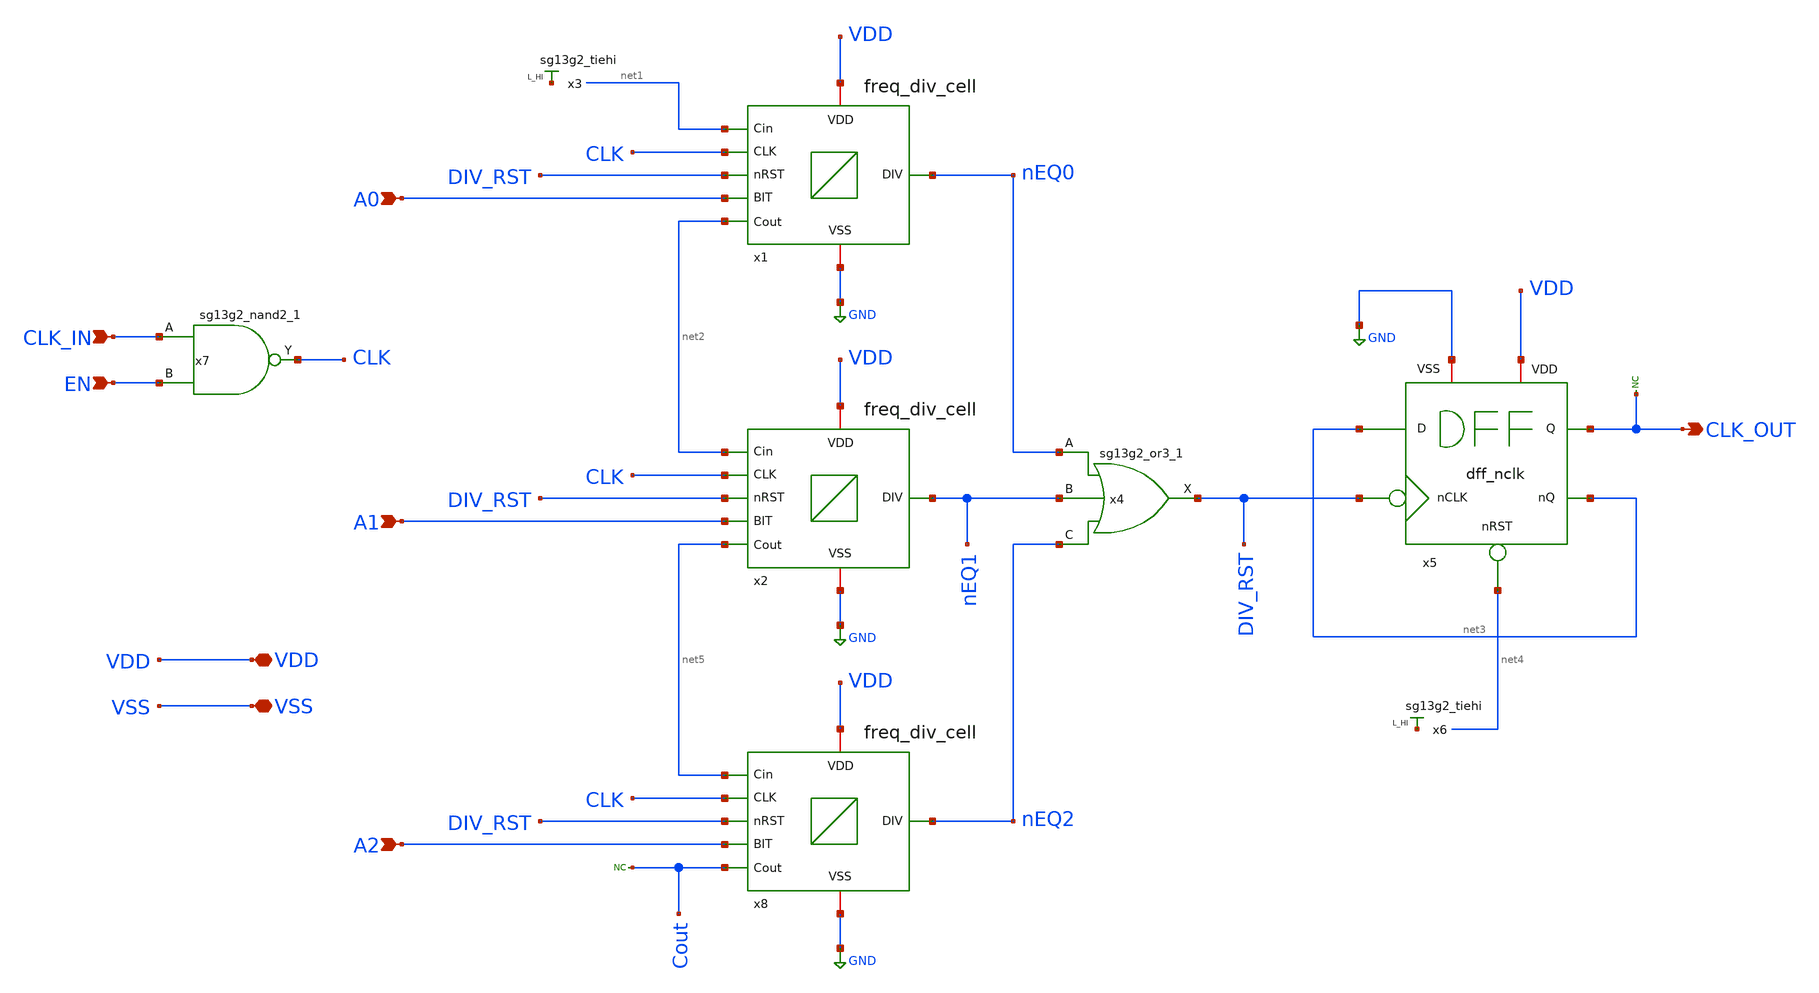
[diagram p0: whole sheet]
** sch_path: Combined Design/design_data/xschem/3bit_freq_divider.sch
* IHP-GmbH/IHP-Open-PDK/ihp-sg13g2/libs.tech/xschem/sg13g2_stdcells/sg13g2_or3_1.sch:
* Copyright 2023 IHP PDK Authors
* Licensed under the Apache License, Version 2.0 (the "License");
**.subckt 3bit_freq_divider CLK_IN EN A0 A1 CLK_OUT VSS VDD A2
*.ipin CLK_IN
*.ipin EN
*.ipin A0
*.ipin A1
*.opin CLK_OUT
*.iopin VSS
*.iopin VDD
*.ipin A2
x1 VDD GND nEQ0 net1 CLK net2 DIV_RST A0 freq_div_cell
x2 VDD GND nEQ1 net2 CLK net5 DIV_RST A1 freq_div_cell
x3 net6 VDD VSS sg13g2_tiehi
x5 DIV_RST CLK_OUT net3 net3 net4 VDD GND dff_nclk
x6 net7 VDD VSS sg13g2_tiehi
* noconn CLK_OUT
x7 CLK CLK_IN EN VDD VSS sg13g2_nand2_1
x4 DIV_RST nEQ0 nEQ1 nEQ2 VDD VSS sg13g2_or3_1
x8 VDD GND nEQ2 net5 CLK Cout DIV_RST A2 freq_div_cell
* noconn Cout
**.ends

* expanding   symbol:  sg13g2_stdcells/sg13g2_nand2_1.sym # of pins=3
** sym_path: sg13g2_stdcells/sg13g2_nand2_1.sym
** sch_path: sg13g2_stdcells/sg13g2_nand2_1.sch
.subckt sg13g2_nand2_1 Y A B VDD VSS
*.iopin VDD
*.iopin VSS
*.ipin A
*.ipin B
*.opin Y
XM1 Y A net1 VSS sg13_lv_nmos w=740.00n l=130.00n ng=1 m=1 mm_ok=1
XM2 net1 B VSS VSS sg13_lv_nmos w=740.00n l=130.00n ng=1 m=1 mm_ok=1
XM3 Y A VDD VDD sg13_lv_pmos w=1.12u l=130.00n ng=1 m=1 mm_ok=1
XM4 Y B VDD VDD sg13_lv_pmos w=1.12u l=130.00n ng=1 m=1 mm_ok=1
.ends


* expanding   symbol:  sg13g2_stdcells/sg13g2_or3_1.sym # of pins=4
** sym_path: sg13g2_stdcells/sg13g2_or3_1.sym
** sch_path: sg13g2_stdcells/sg13g2_or3_1.sch
.subckt sg13g2_or3_1 X A B C VDD VSS
*.opin X
*.ipin C
*.ipin B
*.ipin A
*.iopin VDD
*.iopin VSS
XM1 net2 A VSS VSS sg13_lv_nmos w=550.00n l=130.00n ng=1 m=1 mm_ok=1
XM2 net2 B VSS VSS sg13_lv_nmos w=550.00n l=130.00n ng=1 m=1 mm_ok=1
XM3 net2 C VSS VSS sg13_lv_nmos w=550.00n l=130.00n ng=1 m=1 mm_ok=1
XM4 X net2 VSS VSS sg13_lv_nmos w=740.00n l=130.00n ng=1 m=1 mm_ok=1
XM5 net1 A VDD VDD sg13_lv_pmos w=1.000u l=130.00n ng=1 m=1 mm_ok=1
XM6 net3 B net1 VDD sg13_lv_pmos w=1.000u l=130.00n ng=1 m=1 mm_ok=1
XM7 net2 C net3 VDD sg13_lv_pmos w=1.000u l=130.00n ng=1 m=1 mm_ok=1
XM8 X net2 VDD VDD sg13_lv_pmos w=1.12u l=130.00n ng=1 m=1 mm_ok=1
.ends

.GLOBAL GND
.end
